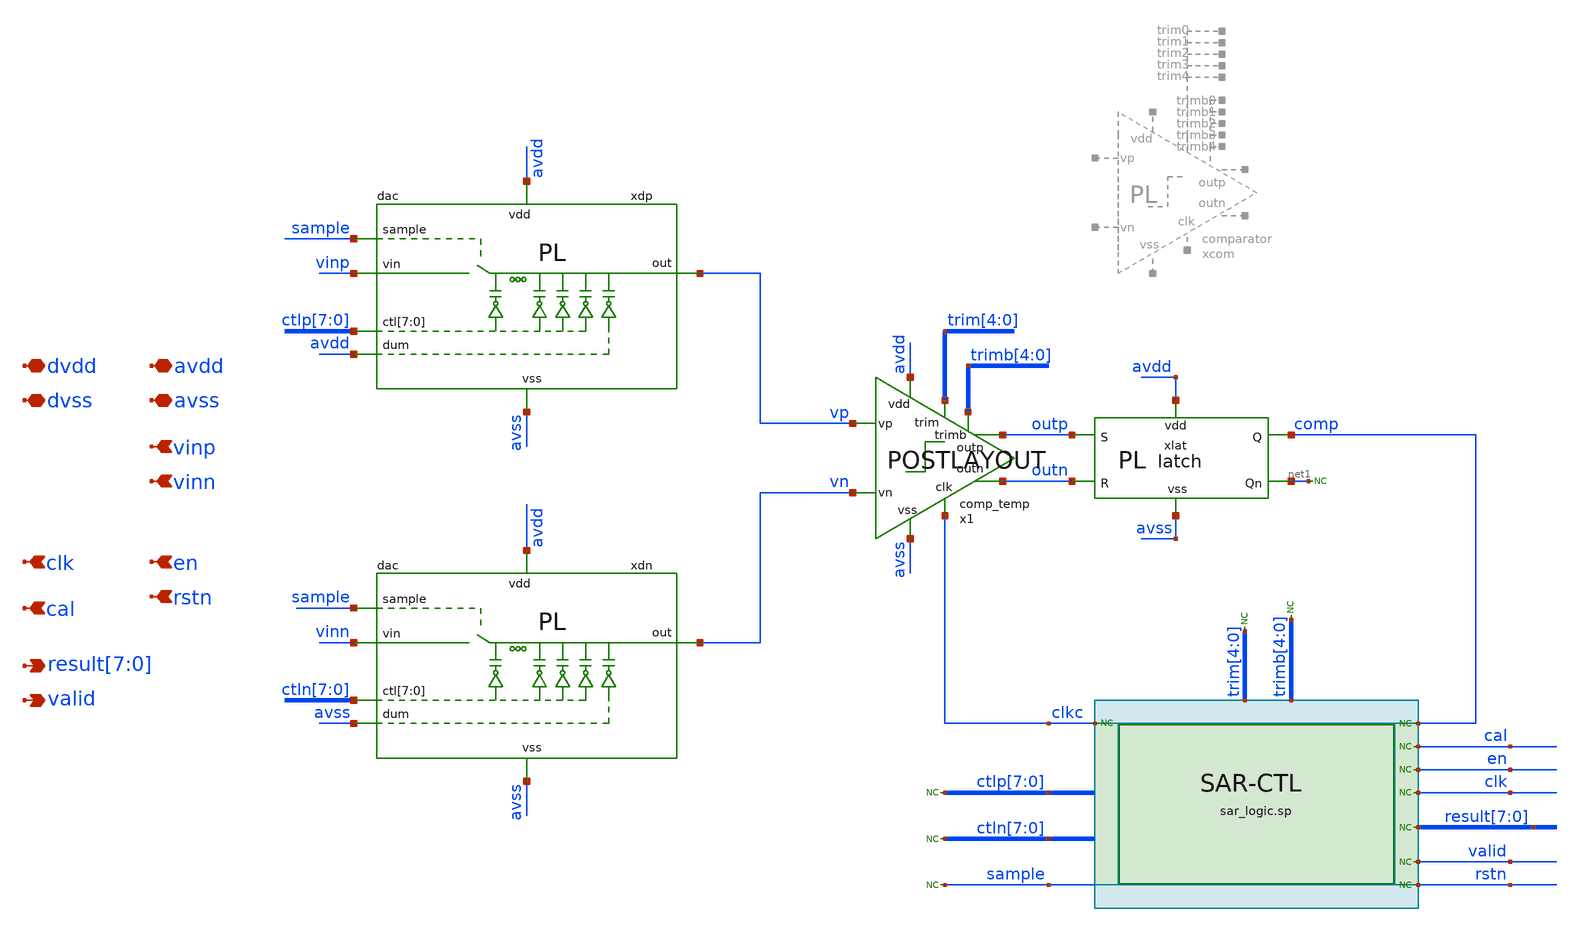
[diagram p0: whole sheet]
** sch_path: xschem/sar/sar/sar.sch
**.subckt sar avss avdd dvss dvdd vinp vinn
*+ result[7],result[6],result[5],result[4],result[3],result[2],result[1],result[0] clk en valid cal rstn
*.iopin avss
*.iopin avdd
*.iopin dvss
*.iopin dvdd
*.ipin vinp
*.ipin vinn
*.opin result[7],result[6],result[5],result[4],result[3],result[2],result[1],result[0]
*.ipin clk
*.ipin en
*.opin valid
*.ipin cal
*.ipin rstn
xlat avdd avss net1 outp outn comp latch
* noconn #net1
* noconn comp
* noconn sample
* noconn ctln[7:0]
* noconn ctlp[7:0]
* noconn trim[4:0]
* noconn trimb[4:0]
* noconn result[7:0]
* noconn valid
* noconn clkc
* noconn clk
* noconn en
* noconn cal
xdn vn sample avdd avss vinn ctln[7] ctln[6] ctln[5] ctln[4] ctln[3] ctln[2] ctln[1] ctln[0] avss
+ dac
xdp vp sample avdd avss vinp ctlp[7] ctlp[6] ctlp[5] ctlp[4] ctlp[3] ctlp[2] ctlp[1] ctlp[0] avdd
+ dac
* noconn rstn
x1 avss avdd clkc outp vp outn vn trim[4] trim[3] trim[2] trim[1] trim[0] trimb[4] trimb[3] trimb[2]
+ trimb[1] trimb[0] comp_temp
**** begin user architecture code

.include $::DESIGN_PATH/sar/control/cmos_cells_digital.sp
.include $::DESIGN_PATH/sar/control/sar_logic.sp



Xuut dclk drstn den dcomp dcal dvalid dres0 dres1 dres2 dres3 dres4 dres5 dres6 dres7 dsamp dctlp0
+ dctlp1 dctlp2 dctlp3 dctlp4 dctlp5 dctlp6 dctlp7 dctln0 dctln1 dctln2 dctln3 dctln4 dctln5 dctln6 dctln7
+ dtrim0 dtrim1 dtrim2 dtrim3 dtrim4 dtrimb0 dtrimb1 dtrimb2 dtrimb3 dtrimb4 dclkc sar_logic

.model adc_buff adc_bridge(in_low = 0.2 in_high=0.8)
.model dac_buff dac_bridge(out_high = 1.2)

Aad [clk rstn en comp cal] [dclk drstn den dcomp dcal] adc_buff
Ada [dctlp0 dctlp1 dctlp2 dctlp3 dctlp4 dctlp5 dctlp6 dctlp7 dctln0 dctln1 dctln2 dctln3 dctln4
+ dctln5 dctln6 dctln7 dres0 dres1 dres2 dres3 dres4 dres5 dres6 dres7 dsamp dclkc] [ctlp_0_ ctlp_1_ ctlp_2_
+ ctlp_3_ ctlp_4_ ctlp_5_ ctlp_6_ ctlp_7_ ctln_0_ ctln_1_ ctln_2_ ctln_3_ ctln_4_ ctln_5_ ctln_6_ ctln_7_
+ res0 res1 res2 res3 res4 res5 res6 res7 sample clkc] dac_buff
Ada2 [dtrim4 dtrim3 dtrim2 dtrim1 dtrim0 dtrimb4 dtrimb3 dtrimb2 dtrimb1 dtrimb0] [trim_4_ trim_3_
+ trim_2_ trim_1_ trim_0_ trimb_4_ trimb_3_ trimb_2_ trimb_1_ trimb_0_ ] dac_buff



**** end user architecture code
**.ends
.end
